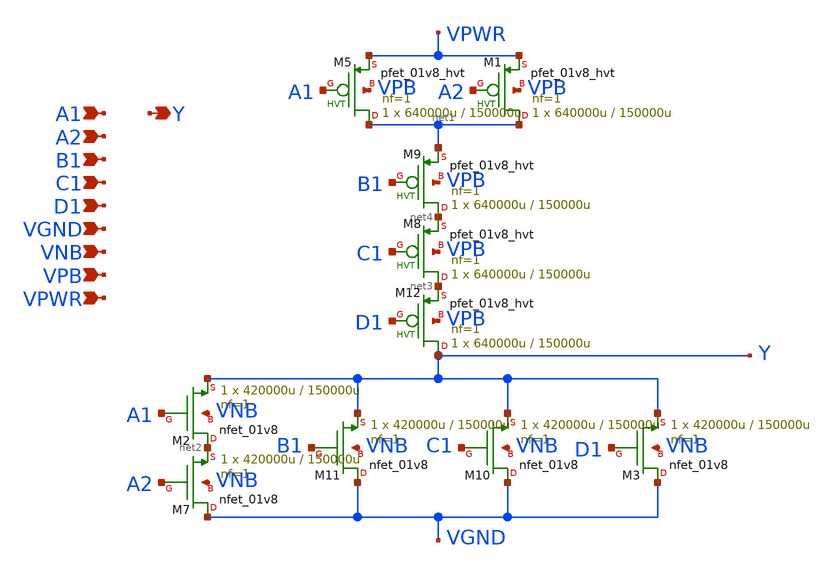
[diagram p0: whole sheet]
** sch_path: schematics/a2111oi/sky130_fd_sc_hd__a2111oi_0.sch
**.subckt sky130_fd_sc_hd__a2111oi_0 A1 A2 B1 C1 D1 VGND VNB VPB VPWR Y
*.ipin A1
*.ipin A2
*.ipin B1
*.ipin C1
*.ipin D1
*.ipin VGND
*.ipin VNB
*.ipin VPB
*.ipin VPWR
*.opin Y
XM1 net1 A2 VPWR VPB sky130_fd_pr__pfet_01v8_hvt L=150000u W=640000u nf=1 ad='int((1 + 1)/2) * 640000u / 1 * 0.29'
+ as='int((1 + 2)/2) * 640000u / 1 * 0.29' pd='2*int((1 + 1)/2) * (640000u / 1 + 0.29)' ps='2*int((1 + 2)/2) * (640000u / 1 + 0.29)'
+ nrd='0.29 / 640000u ' nrs='0.29 / 640000u ' sa=0 sb=0 sd=0 mult=1 m=1
XM2 net2 A1 Y VNB sky130_fd_pr__nfet_01v8 L=150000u W=420000u nf=1 ad='int((1 + 1)/2) * 420000u / 1 * 0.29'
+ as='int((1 + 2)/2) * 420000u / 1 * 0.29' pd='2*int((1 + 1)/2) * (420000u / 1 + 0.29)' ps='2*int((1 + 2)/2) * (420000u / 1 + 0.29)'
+ nrd='0.29 / 420000u ' nrs='0.29 / 420000u ' sa=0 sb=0 sd=0 mult=1 m=1
XM3 VGND D1 Y VNB sky130_fd_pr__nfet_01v8 L=150000u W=420000u nf=1 ad='int((1 + 1)/2) * 420000u / 1 * 0.29'
+ as='int((1 + 2)/2) * 420000u / 1 * 0.29' pd='2*int((1 + 1)/2) * (420000u / 1 + 0.29)' ps='2*int((1 + 2)/2) * (420000u / 1 + 0.29)'
+ nrd='0.29 / 420000u ' nrs='0.29 / 420000u ' sa=0 sb=0 sd=0 mult=1 m=1
XM5 net1 A1 VPWR VPB sky130_fd_pr__pfet_01v8_hvt L=150000u W=640000u nf=1 ad='int((1 + 1)/2) * 640000u / 1 * 0.29'
+ as='int((1 + 2)/2) * 640000u / 1 * 0.29' pd='2*int((1 + 1)/2) * (640000u / 1 + 0.29)' ps='2*int((1 + 2)/2) * (640000u / 1 + 0.29)'
+ nrd='0.29 / 640000u ' nrs='0.29 / 640000u ' sa=0 sb=0 sd=0 mult=1 m=1
XM8 net3 C1 net4 VPB sky130_fd_pr__pfet_01v8_hvt L=150000u W=640000u nf=1 ad='int((1 + 1)/2) * 640000u / 1 * 0.29'
+ as='int((1 + 2)/2) * 640000u / 1 * 0.29' pd='2*int((1 + 1)/2) * (640000u / 1 + 0.29)' ps='2*int((1 + 2)/2) * (640000u / 1 + 0.29)'
+ nrd='0.29 / 640000u ' nrs='0.29 / 640000u ' sa=0 sb=0 sd=0 mult=1 m=1
XM9 net4 B1 net1 VPB sky130_fd_pr__pfet_01v8_hvt L=150000u W=640000u nf=1 ad='int((1 + 1)/2) * 640000u / 1 * 0.29'
+ as='int((1 + 2)/2) * 640000u / 1 * 0.29' pd='2*int((1 + 1)/2) * (640000u / 1 + 0.29)' ps='2*int((1 + 2)/2) * (640000u / 1 + 0.29)'
+ nrd='0.29 / 640000u ' nrs='0.29 / 640000u ' sa=0 sb=0 sd=0 mult=1 m=1
XM7 VGND A2 net2 VNB sky130_fd_pr__nfet_01v8 L=150000u W=420000u nf=1 ad='int((1 + 1)/2) * 420000u / 1 * 0.29'
+ as='int((1 + 2)/2) * 420000u / 1 * 0.29' pd='2*int((1 + 1)/2) * (420000u / 1 + 0.29)' ps='2*int((1 + 2)/2) * (420000u / 1 + 0.29)'
+ nrd='0.29 / 420000u ' nrs='0.29 / 420000u ' sa=0 sb=0 sd=0 mult=1 m=1
XM10 VGND C1 Y VNB sky130_fd_pr__nfet_01v8 L=150000u W=420000u nf=1 ad='int((1 + 1)/2) * 420000u / 1 * 0.29'
+ as='int((1 + 2)/2) * 420000u / 1 * 0.29' pd='2*int((1 + 1)/2) * (420000u / 1 + 0.29)' ps='2*int((1 + 2)/2) * (420000u / 1 + 0.29)'
+ nrd='0.29 / 420000u ' nrs='0.29 / 420000u ' sa=0 sb=0 sd=0 mult=1 m=1
XM11 VGND B1 Y VNB sky130_fd_pr__nfet_01v8 L=150000u W=420000u nf=1 ad='int((1 + 1)/2) * 420000u / 1 * 0.29'
+ as='int((1 + 2)/2) * 420000u / 1 * 0.29' pd='2*int((1 + 1)/2) * (420000u / 1 + 0.29)' ps='2*int((1 + 2)/2) * (420000u / 1 + 0.29)'
+ nrd='0.29 / 420000u ' nrs='0.29 / 420000u ' sa=0 sb=0 sd=0 mult=1 m=1
XM12 Y D1 net3 VPB sky130_fd_pr__pfet_01v8_hvt L=150000u W=640000u nf=1 ad='int((1 + 1)/2) * 640000u / 1 * 0.29'
+ as='int((1 + 2)/2) * 640000u / 1 * 0.29' pd='2*int((1 + 1)/2) * (640000u / 1 + 0.29)' ps='2*int((1 + 2)/2) * (640000u / 1 + 0.29)'
+ nrd='0.29 / 640000u ' nrs='0.29 / 640000u ' sa=0 sb=0 sd=0 mult=1 m=1
**.ends
.end
